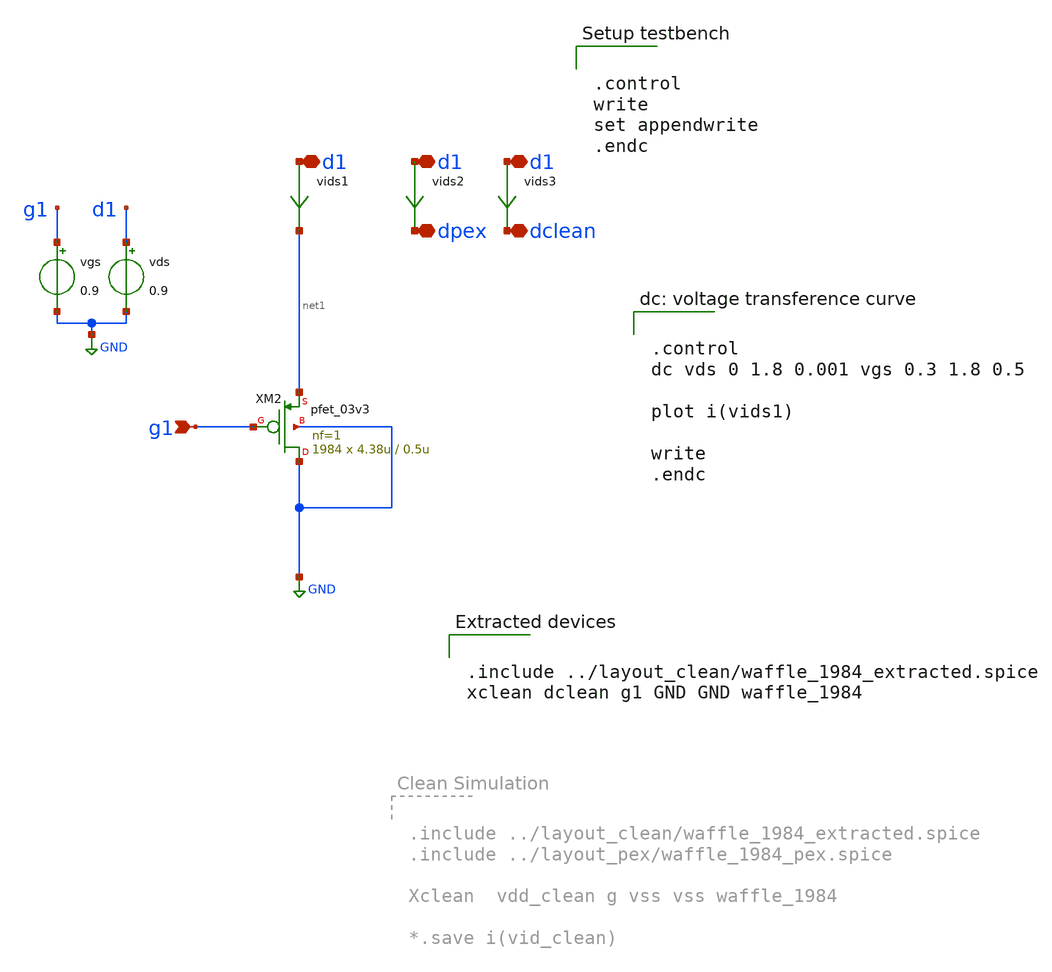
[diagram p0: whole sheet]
** sch_path: LDO/xschem/waffle_1984/test/nmos_charac_pex.sch

.control
write
set appendwrite
.endc



.include $env(PDK_ROOT)/$env(PDK)/libs.tech/ngspice/design.ngspice
.lib $env(PDK_ROOT)/$env(PDK)/libs.tech/ngspice/sm141064.ngspice typical
.lib $env(PDK_ROOT)/$env(PDK)/libs.tech/ngspice/sm141064.ngspice mimcap_statistical
.lib $env(PDK_ROOT)/$env(PDK)/libs.tech/ngspice/sm141064.ngspice cap_mim
.lib $env(PDK_ROOT)/$env(PDK)/libs.tech/ngspice/sm141064.ngspice res_typical
.lib $env(PDK_ROOT)/$env(PDK)/libs.tech/ngspice/sm141064.ngspice bjt_typical
.lib $env(PDK_ROOT)/$env(PDK)/libs.tech/ngspice/sm141064.ngspice moscap_typical

**.subckt nmos_charac_pex g1 d1 d1 dpex d1 dclean
*.ipin g1
*.iopin d1
*.iopin d1
*.iopin dpex
*.iopin d1
*.iopin dclean
vgs g1 GND 0.9
vds d1 GND 0.9
vids1 d1 net1 0
.save i(vids1)
vids2 d1 dpex 0
.save i(vids2)
XM2 GND g1 net1 GND pfet_03v3 L=0.5u W=4.38u nf=1 ad='int((nf+1)/2) * W/nf * 0.18u' as='int((nf+2)/2) * W/nf * 0.18u'
+ pd='2*int((nf+1)/2) * (W/nf + 0.18u)' ps='2*int((nf+2)/2) * (W/nf + 0.18u)' nrd='0.18u / W' nrs='0.18u / W'
+ sa=0 sb=0 sd=0 m=1984
vids3 d1 dclean 0
.save i(vids3)
**** begin user architecture code


.control
dc vds 0 1.8 0.001 vgs 0.3 1.8 0.5

plot i(vids1)

write
.endc




.include ../layout_clean/waffle_1984_extracted.spice
xclean dclean g1 GND GND waffle_1984


**** end user architecture code
**.ends
.GLOBAL GND
.end
